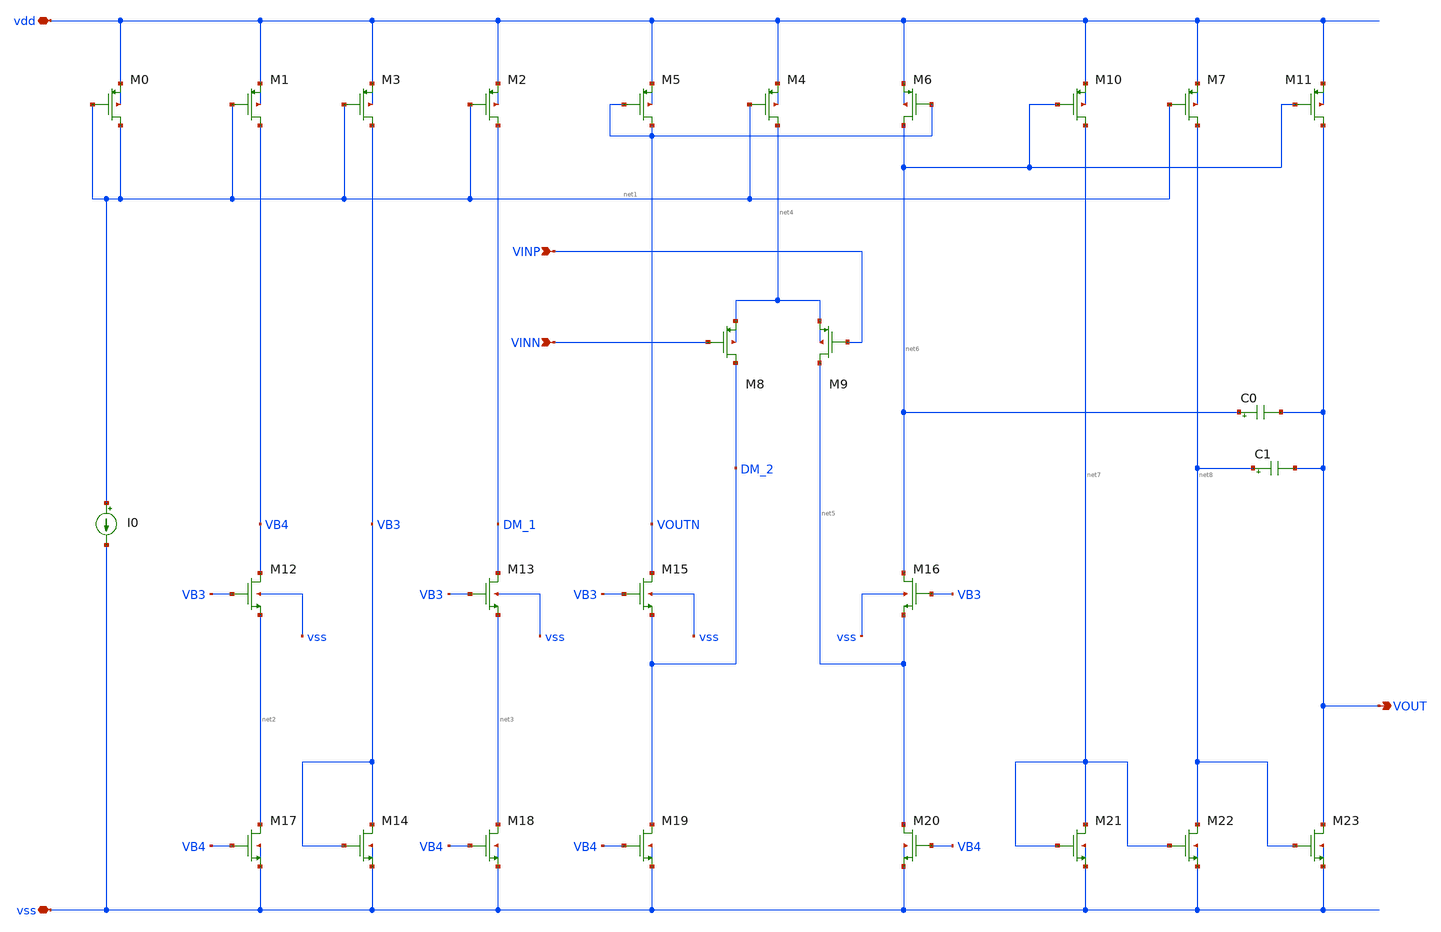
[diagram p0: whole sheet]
** sch_path: analog-db/drawings/publication/amp_008_leung_nmcf.sch
**.subckt amp_008_leung_nmcf vdd vss VINN VINP VOUT
*.iopin vdd
*.iopin vss
*.ipin VINN
*.ipin VINP
*.opin VOUT
XM0 net1 net1 vdd vdd sg13_lv_pmos w=x_dut_xm0_w l=x_dut_xm0_l ng=1 m=x_dut_xm0_m mm_ok=1
XM1 VB4 net1 vdd vdd sg13_lv_pmos w=x_dut_xm1_w l=x_dut_xm1_l ng=1 m=x_dut_xm1_m mm_ok=1
XM3 VB3 net1 vdd vdd sg13_lv_pmos w=x_dut_xm3_w l=x_dut_xm3_l ng=1 m=x_dut_xm3_m mm_ok=1
XM2 DM_1 net1 vdd vdd sg13_lv_pmos w=x_dut_xm2_w l=x_dut_xm2_l ng=1 m=x_dut_xm2_m mm_ok=1
XM12 VB4 VB3 net2 vss sg13_lv_nmos w=x_dut_xm12_w l=x_dut_xm12_l ng=1 m=x_dut_xm12_m mm_ok=1
XM13 DM_1 VB3 net3 vss sg13_lv_nmos w=x_dut_xm13_w l=x_dut_xm13_l ng=1 m=x_dut_xm13_m mm_ok=1
XM17 net2 VB4 vss vss sg13_lv_nmos w=x_dut_xm17_w l=x_dut_xm17_l ng=1 m=x_dut_xm17_m mm_ok=1
XM14 VB3 VB3 vss vss sg13_lv_nmos w=x_dut_xm14_w l=x_dut_xm14_l ng=1 m=x_dut_xm14_m mm_ok=1
XM18 net3 VB4 vss vss sg13_lv_nmos w=x_dut_xm18_w l=x_dut_xm18_l ng=1 m=x_dut_xm18_m mm_ok=1
XM5 VOUTN VOUTN vdd vdd sg13_lv_pmos w=x_dut_xm5_w l=x_dut_xm5_l ng=1 m=x_dut_xm5_m mm_ok=1
XM4 net4 net1 vdd vdd sg13_lv_pmos w=x_dut_xm4_w l=x_dut_xm4_l ng=1 m=x_dut_xm4_m mm_ok=1
XM6 net6 VOUTN vdd vdd sg13_lv_pmos w=x_dut_xm6_w l=x_dut_xm6_l ng=1 m=x_dut_xm6_m mm_ok=1
XM8 DM_2 VINN net4 net4 sg13_lv_pmos w=x_dut_xm8_w l=x_dut_xm8_l ng=1 m=x_dut_xm8_m mm_ok=1
XM9 net5 VINP net4 net4 sg13_lv_pmos w=x_dut_xm9_w l=x_dut_xm9_l ng=1 m=x_dut_xm9_m mm_ok=1
XM15 VOUTN VB3 DM_2 vss sg13_lv_nmos w=x_dut_xm15_w l=x_dut_xm15_l ng=1 m=x_dut_xm15_m mm_ok=1
XM16 net6 VB3 net5 vss sg13_lv_nmos w=x_dut_xm16_w l=x_dut_xm16_l ng=1 m=x_dut_xm16_m mm_ok=1
XM19 DM_2 VB4 vss vss sg13_lv_nmos w=x_dut_xm19_w l=x_dut_xm19_l ng=1 m=x_dut_xm19_m mm_ok=1
XM20 net5 VB4 vss vss sg13_lv_nmos w=x_dut_xm20_w l=x_dut_xm20_l ng=1 m=x_dut_xm20_m mm_ok=1
XM10 net7 net6 vdd vdd sg13_lv_pmos w=x_dut_xm10_w l=x_dut_xm10_l ng=1 m=x_dut_xm10_m mm_ok=1
XM7 net8 net1 vdd vdd sg13_lv_pmos w=x_dut_xm7_w l=x_dut_xm7_l ng=1 m=x_dut_xm7_m mm_ok=1
XM21 net7 net7 vss vss sg13_lv_nmos w=x_dut_xm21_w l=x_dut_xm21_l ng=1 m=x_dut_xm21_m mm_ok=1
XM22 net8 net7 vss vss sg13_lv_nmos w=x_dut_xm22_w l=x_dut_xm22_l ng=1 m=x_dut_xm22_m mm_ok=1
XM11 VOUT net6 vdd vdd sg13_lv_pmos w=x_dut_xm11_w l=x_dut_xm11_l ng=1 m=x_dut_xm11_m mm_ok=1
XM23 VOUT net8 vss vss sg13_lv_nmos w=x_dut_xm23_w l=x_dut_xm23_l ng=1 m=x_dut_xm23_m mm_ok=1
I0 net1 vss 'CURRENT_0_BIAS'
C0 net6 VOUT 'CAPACITOR_0' m=1
C1 net8 VOUT 'CAPACITOR_1' m=1
**.ends
.end
